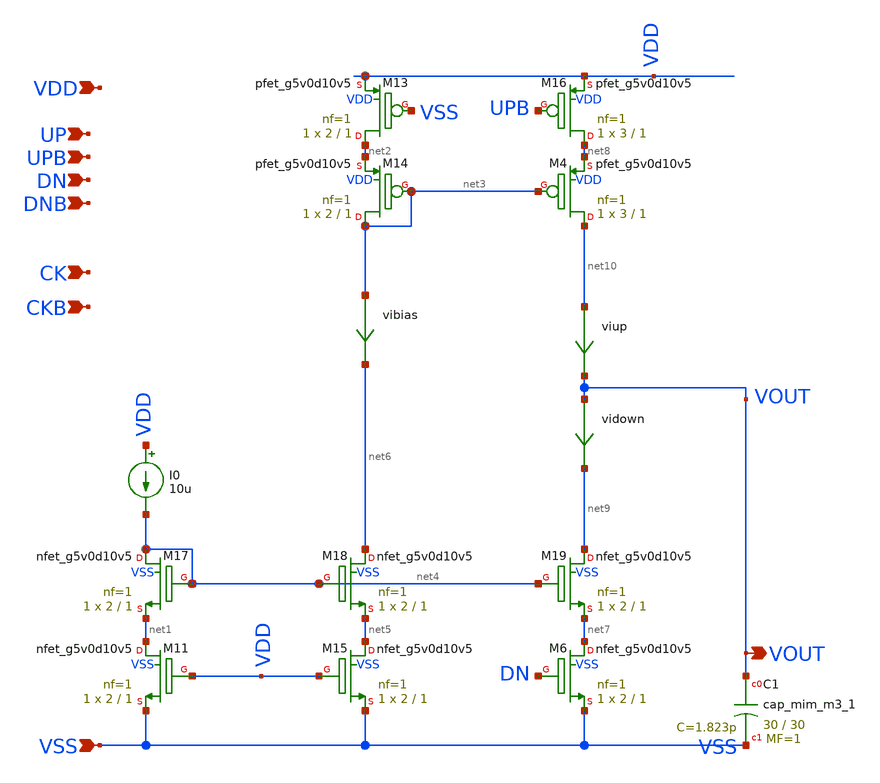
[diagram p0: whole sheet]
** sch_path: xschem/pll_cp_delta_hv.sch
**.subckt pll_cp_delta_hv VOUT VSS UP DNB CK CKB VDD DN UPB
*.opin VOUT
*.ipin VSS
*.ipin UP
*.ipin DNB
*.ipin CK
*.ipin CKB
*.ipin VDD
*.ipin DN
*.ipin UPB
XC1 VOUT VSS sky130_fd_pr__cap_mim_m3_1 W=30 L=30 MF=1 m=1
vibias net3 net6 0
.save i(vibias)
XM16 net8 UPB VDD VDD sky130_fd_pr__pfet_g5v0d10v5 L=1 W=3 nf=1 ad='int((nf+1)/2) * W/nf * 0.29' as='int((nf+2)/2) * W/nf * 0.29'
+ pd='2*int((nf+1)/2) * (W/nf + 0.29)' ps='2*int((nf+2)/2) * (W/nf + 0.29)' nrd='0.29 / W' nrs='0.29 / W'
+ sa=0 sb=0 sd=0 mult=1 m=1
XM13 net2 VSS VDD VDD sky130_fd_pr__pfet_g5v0d10v5 L=1 W=2 nf=1 ad='int((nf+1)/2) * W/nf * 0.29' as='int((nf+2)/2) * W/nf * 0.29'
+ pd='2*int((nf+1)/2) * (W/nf + 0.29)' ps='2*int((nf+2)/2) * (W/nf + 0.29)' nrd='0.29 / W' nrs='0.29 / W'
+ sa=0 sb=0 sd=0 mult=1 m=1
XM14 net3 net3 net2 VDD sky130_fd_pr__pfet_g5v0d10v5 L=1 W=2 nf=1 ad='int((nf+1)/2) * W/nf * 0.29' as='int((nf+2)/2) * W/nf * 0.29'
+ pd='2*int((nf+1)/2) * (W/nf + 0.29)' ps='2*int((nf+2)/2) * (W/nf + 0.29)' nrd='0.29 / W' nrs='0.29 / W'
+ sa=0 sb=0 sd=0 mult=1 m=1
I0 VDD net4 10u
XM11 net1 VDD VSS VSS sky130_fd_pr__nfet_g5v0d10v5 L=1 W=2 nf=1 ad='int((nf+1)/2) * W/nf * 0.29' as='int((nf+2)/2) * W/nf * 0.29'
+ pd='2*int((nf+1)/2) * (W/nf + 0.29)' ps='2*int((nf+2)/2) * (W/nf + 0.29)' nrd='0.29 / W' nrs='0.29 / W'
+ sa=0 sb=0 sd=0 mult=1 m=1
XM17 net4 net4 net1 VSS sky130_fd_pr__nfet_g5v0d10v5 L=1 W=2 nf=1 ad='int((nf+1)/2) * W/nf * 0.29' as='int((nf+2)/2) * W/nf * 0.29'
+ pd='2*int((nf+1)/2) * (W/nf + 0.29)' ps='2*int((nf+2)/2) * (W/nf + 0.29)' nrd='0.29 / W' nrs='0.29 / W'
+ sa=0 sb=0 sd=0 mult=1 m=1
XM15 net5 VDD VSS VSS sky130_fd_pr__nfet_g5v0d10v5 L=1 W=2 nf=1 ad='int((nf+1)/2) * W/nf * 0.29' as='int((nf+2)/2) * W/nf * 0.29'
+ pd='2*int((nf+1)/2) * (W/nf + 0.29)' ps='2*int((nf+2)/2) * (W/nf + 0.29)' nrd='0.29 / W' nrs='0.29 / W'
+ sa=0 sb=0 sd=0 mult=1 m=1
XM18 net6 net4 net5 VSS sky130_fd_pr__nfet_g5v0d10v5 L=1 W=2 nf=1 ad='int((nf+1)/2) * W/nf * 0.29' as='int((nf+2)/2) * W/nf * 0.29'
+ pd='2*int((nf+1)/2) * (W/nf + 0.29)' ps='2*int((nf+2)/2) * (W/nf + 0.29)' nrd='0.29 / W' nrs='0.29 / W'
+ sa=0 sb=0 sd=0 mult=1 m=1
XM6 net7 DN VSS VSS sky130_fd_pr__nfet_g5v0d10v5 L=1 W=2 nf=1 ad='int((nf+1)/2) * W/nf * 0.29' as='int((nf+2)/2) * W/nf * 0.29'
+ pd='2*int((nf+1)/2) * (W/nf + 0.29)' ps='2*int((nf+2)/2) * (W/nf + 0.29)' nrd='0.29 / W' nrs='0.29 / W'
+ sa=0 sb=0 sd=0 mult=1 m=1
XM19 net9 net4 net7 VSS sky130_fd_pr__nfet_g5v0d10v5 L=1 W=2 nf=1 ad='int((nf+1)/2) * W/nf * 0.29' as='int((nf+2)/2) * W/nf * 0.29'
+ pd='2*int((nf+1)/2) * (W/nf + 0.29)' ps='2*int((nf+2)/2) * (W/nf + 0.29)' nrd='0.29 / W' nrs='0.29 / W'
+ sa=0 sb=0 sd=0 mult=1 m=1
XM4 net10 net3 net8 VDD sky130_fd_pr__pfet_g5v0d10v5 L=1 W=3 nf=1 ad='int((nf+1)/2) * W/nf * 0.29' as='int((nf+2)/2) * W/nf * 0.29'
+ pd='2*int((nf+1)/2) * (W/nf + 0.29)' ps='2*int((nf+2)/2) * (W/nf + 0.29)' nrd='0.29 / W' nrs='0.29 / W'
+ sa=0 sb=0 sd=0 mult=1 m=1
viup net10 VOUT 0
.save i(viup)
vidown VOUT net9 0
.save i(vidown)
**.ends
.end
